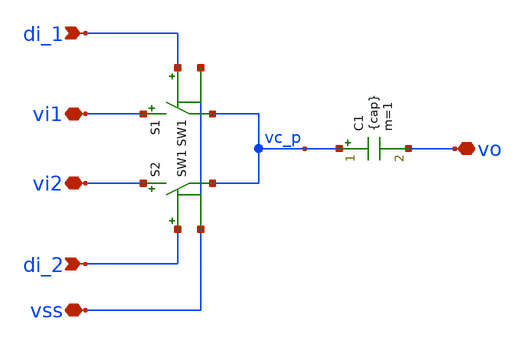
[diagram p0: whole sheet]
** sch_path: xschem/sw_cap.sch
**.subckt sw_cap di_1 di_2 vi1 vi2 vo vss
*.ipin di_1
*.ipin di_2
*.iopin vi1
*.iopin vi2
*.iopin vo
*.iopin vss
C1 vc_p vo {cap} m=1
S1 vi1 vc_p di_1 vss SW1
S2 vi2 vc_p di_2 vss SW1
**.ends
**** begin user architecture code
.MODEL SW1 SW( VT=0.75 VH=0.01 RON=ron ROFF=roff )
**** end user architecture code
.end
